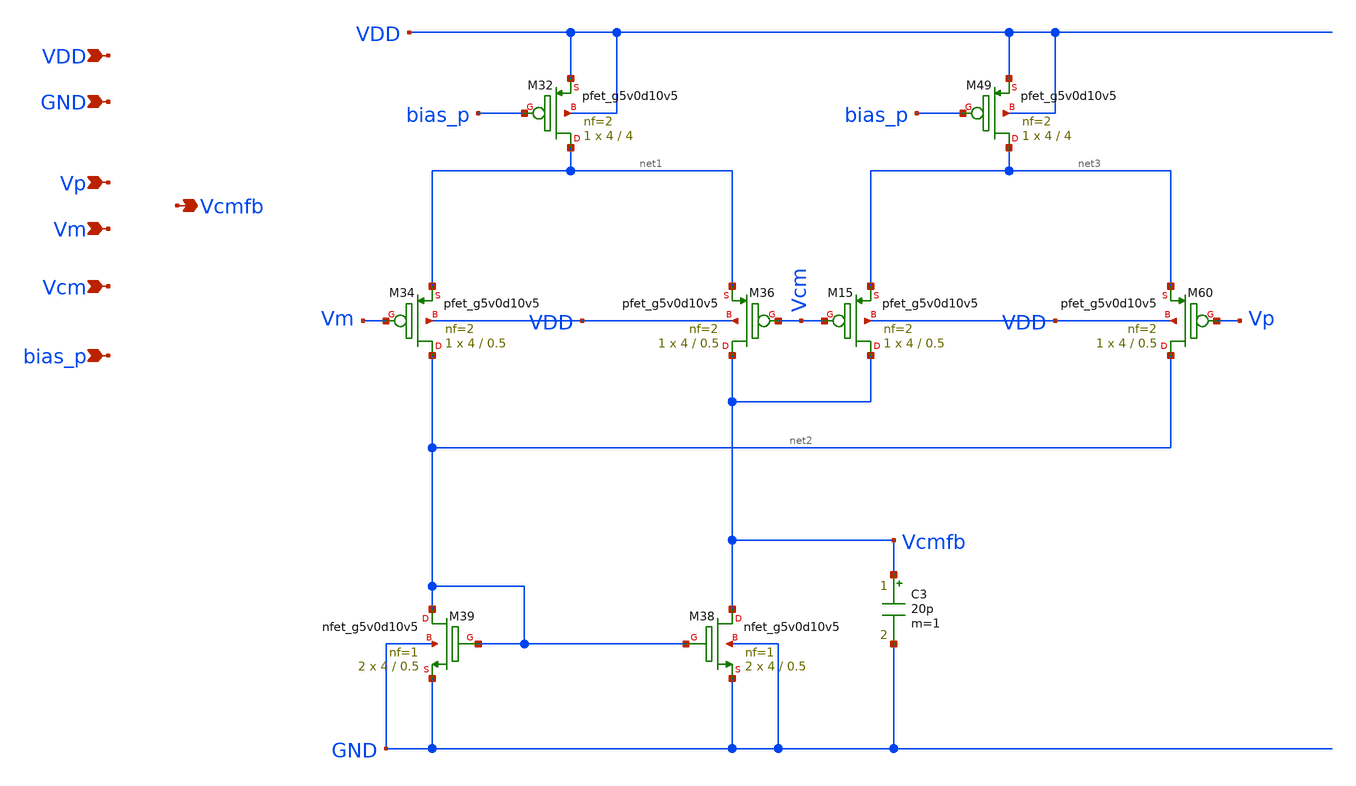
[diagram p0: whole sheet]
** sch_path: xschem/cmfb.sch
**.subckt cmfb Vp Vm VDD Vcmfb GND Vcm bias_p
*.ipin Vp
*.ipin Vm
*.ipin VDD
*.opin Vcmfb
*.ipin GND
*.ipin Vcm
*.ipin bias_p
XM32 net1 bias_p VDD VDD sky130_fd_pr__pfet_g5v0d10v5 L=4 W=4 nf=2 ad='int((nf+1)/2) * W/nf * 0.29' as='int((nf+2)/2) * W/nf * 0.29'
+ pd='2*int((nf+1)/2) * (W/nf + 0.29)' ps='2*int((nf+2)/2) * (W/nf + 0.29)' nrd='0.29 / W' nrs='0.29 / W'
+ sa=0 sb=0 sd=0 mult=1 m=1
XM34 net2 Vm net1 VDD sky130_fd_pr__pfet_g5v0d10v5 L=0.5 W=4 nf=2 ad='int((nf+1)/2) * W/nf * 0.29' as='int((nf+2)/2) * W/nf * 0.29'
+ pd='2*int((nf+1)/2) * (W/nf + 0.29)' ps='2*int((nf+2)/2) * (W/nf + 0.29)' nrd='0.29 / W' nrs='0.29 / W'
+ sa=0 sb=0 sd=0 mult=1 m=1
XM36 Vcmfb Vcm net1 VDD sky130_fd_pr__pfet_g5v0d10v5 L=0.5 W=4 nf=2 ad='int((nf+1)/2) * W/nf * 0.29'
+ as='int((nf+2)/2) * W/nf * 0.29' pd='2*int((nf+1)/2) * (W/nf + 0.29)' ps='2*int((nf+2)/2) * (W/nf + 0.29)'
+ nrd='0.29 / W' nrs='0.29 / W' sa=0 sb=0 sd=0 mult=1 m=1
XM38 Vcmfb net2 GND GND sky130_fd_pr__nfet_g5v0d10v5 L=0.5 W=4 nf=1 ad='int((nf+1)/2) * W/nf * 0.29'
+ as='int((nf+2)/2) * W/nf * 0.29' pd='2*int((nf+1)/2) * (W/nf + 0.29)' ps='2*int((nf+2)/2) * (W/nf + 0.29)'
+ nrd='0.29 / W' nrs='0.29 / W' sa=0 sb=0 sd=0 mult=2 m=2
XM39 net2 net2 GND GND sky130_fd_pr__nfet_g5v0d10v5 L=0.5 W=4 nf=1 ad='int((nf+1)/2) * W/nf * 0.29' as='int((nf+2)/2) * W/nf * 0.29'
+ pd='2*int((nf+1)/2) * (W/nf + 0.29)' ps='2*int((nf+2)/2) * (W/nf + 0.29)' nrd='0.29 / W' nrs='0.29 / W'
+ sa=0 sb=0 sd=0 mult=2 m=2
C3 Vcmfb GND 20p m=1
XM15 Vcmfb Vcm net3 VDD sky130_fd_pr__pfet_g5v0d10v5 L=0.5 W=4 nf=2 ad='int((nf+1)/2) * W/nf * 0.29'
+ as='int((nf+2)/2) * W/nf * 0.29' pd='2*int((nf+1)/2) * (W/nf + 0.29)' ps='2*int((nf+2)/2) * (W/nf + 0.29)'
+ nrd='0.29 / W' nrs='0.29 / W' sa=0 sb=0 sd=0 mult=1 m=1
XM49 net3 bias_p VDD VDD sky130_fd_pr__pfet_g5v0d10v5 L=4 W=4 nf=2 ad='int((nf+1)/2) * W/nf * 0.29' as='int((nf+2)/2) * W/nf * 0.29'
+ pd='2*int((nf+1)/2) * (W/nf + 0.29)' ps='2*int((nf+2)/2) * (W/nf + 0.29)' nrd='0.29 / W' nrs='0.29 / W'
+ sa=0 sb=0 sd=0 mult=1 m=1
XM60 net2 Vp net3 VDD sky130_fd_pr__pfet_g5v0d10v5 L=0.5 W=4 nf=2 ad='int((nf+1)/2) * W/nf * 0.29' as='int((nf+2)/2) * W/nf * 0.29'
+ pd='2*int((nf+1)/2) * (W/nf + 0.29)' ps='2*int((nf+2)/2) * (W/nf + 0.29)' nrd='0.29 / W' nrs='0.29 / W'
+ sa=0 sb=0 sd=0 mult=1 m=1
**.ends
.end
